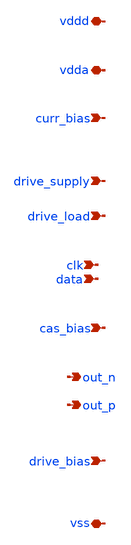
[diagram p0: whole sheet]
** sch_path: design/dac_unit_cell/dac_unit_cell_pex.sch
**.subckt dac_unit_cell_pex vdda vss curr_bias drive_supply cas_bias drive_bias drive_load vddd clk
*+ data out_p out_n
*.iopin vdda
*.iopin vss
*.ipin curr_bias
*.ipin drive_supply
*.ipin cas_bias
*.ipin drive_bias
*.ipin drive_load
*.iopin vddd
*.ipin clk
*.ipin data
*.opin out_p
*.opin out_n
**** begin user architecture code



xpex vdda curr_bias clk data out_p out_n drive_load vss drive_supply cas_bias drive_bias vddd
+ dac_unit_cell_pex_sub

* NGSPICE file created from dac_unit_cell.ext - technology: sky130A

.subckt sky130_fd_pr__nfet_01v8_lvt_0-42_8-00 a_n800_n130# a_n858_n42# a_800_n42#  w_n884_n68#
X0 a_800_n42# a_n800_n130# a_n858_n42# w_n884_n68# sky130_fd_pr__nfet_01v8_lvt ad=1.218e+11p
+ pd=1.42e+06u as=1.218e+11p ps=1.42e+06u w=420000u l=8e+06u
C0 a_800_n42# w_n884_n68# 0.03fF
C1 a_n858_n42# w_n884_n68# 0.03fF
C2 a_n800_n130# w_n884_n68# 1.73fF
.ends

.subckt sky130_fd_pr__pfet_01v8_0-84_0-15 VSUBS a_15_n84# w_n109_n184# a_n33_n181#  a_n73_n84#
X0 a_15_n84# a_n33_n181# a_n73_n84# w_n109_n184# sky130_fd_pr__pfet_01v8 ad=2.436e+11p pd=2.26e+06u
+ as=2.436e+11p ps=2.26e+06u w=840000u l=150000u
C0 a_15_n84# a_n73_n84# 0.29fF
C1 a_15_n84# a_n33_n181# 0.03fF
C2 a_n33_n181# a_n73_n84# 0.03fF
C3 a_15_n84# VSUBS 0.03fF
C4 a_n73_n84# VSUBS 0.03fF
C5 a_n33_n181# VSUBS 0.20fF
C6 w_n109_n184# VSUBS 0.24fF
.ends

.subckt sky130_fd_sc_hs__inv_1 VGND Y VPWR A VPB VNB
X0 Y A VPWR VPB sky130_fd_pr__pfet_01v8 ad=3.304e+11p pd=2.83e+06u as=3.864e+11p ps=2.93e+06u
+ w=1.12e+06u l=150000u
X1 Y A VGND VNB sky130_fd_pr__nfet_01v8_lvt ad=2.109e+11p pd=2.05e+06u as=2.627e+11p ps=2.19e+06u
+ w=740000u l=150000u
C0 VPWR VGND 0.01fF
C1 A VGND 0.08fF
C2 VPWR VPB 0.02fF
C3 Y VPWR 0.24fF
C4 Y A 0.26fF
C5 A VPWR 0.08fF
C6 Y VGND 0.19fF
C7 VGND VNB 0.37fF
C8 Y VNB 0.19fF
C9 VPWR VNB 0.36fF
C10 A VNB 0.36fF
C11 VPB VNB 0.41fF
.ends

.subckt sky130_fd_sc_hs__dfxtp_1 a_713_458# Q a_454_503# VGND a_1118_508# a_668_503#  a_206_368#
+ a_27_74# VPWR CLK a_731_101# a_561_463# VPB a_1168_124# VNB a_1210_314#  D a_1011_424#
X0 VPWR CLK a_27_74# VPB sky130_fd_pr__pfet_01v8 ad=1.50923e+12p pd=1.272e+07u as=3.304e+11p
+ ps=2.83e+06u w=1.12e+06u l=150000u
X1 a_561_463# a_206_368# a_454_503# VPB sky130_fd_pr__pfet_01v8 ad=1.967e+11p pd=2.01e+06u
+ as=1.967e+11p ps=2.01e+06u w=420000u l=150000u
X2 VPWR a_1210_314# a_1118_508# VPB sky130_fd_pr__pfet_01v8 ad=0p pd=0u as=1.995e+11p ps=1.79e+06u
+ w=420000u l=150000u
X3 a_713_458# a_561_463# VPWR VPB sky130_fd_pr__pfet_01v8 ad=4.662e+11p pd=2.79e+06u as=0p ps=0u
+ w=840000u l=150000u
X4 VPWR a_1011_424# a_1210_314# VPB sky130_fd_pr__pfet_01v8 ad=0p pd=0u as=2.478e+11p ps=2.27e+06u
+ w=840000u l=150000u
X5 Q a_1210_314# VPWR VPB sky130_fd_pr__pfet_01v8 ad=3.304e+11p pd=2.83e+06u as=0p ps=0u w=1.12e+06u
+ l=150000u
X6 Q a_1210_314# VGND VNB sky130_fd_pr__nfet_01v8_lvt ad=2.109e+11p pd=2.05e+06u as=1.27305e+12p
+ ps=1.059e+07u w=740000u l=150000u
X7 a_668_503# a_27_74# a_561_463# VPB sky130_fd_pr__pfet_01v8 ad=1.008e+11p pd=1.32e+06u as=0p ps=0u
+ w=420000u l=150000u
X8 VGND a_1011_424# a_1210_314# VNB sky130_fd_pr__nfet_01v8_lvt ad=0p pd=0u as=1.824e+11p
+ ps=1.85e+06u w=640000u l=150000u
X9 a_731_101# a_206_368# a_561_463# VNB sky130_fd_pr__nfet_01v8_lvt ad=8.82e+10p pd=1.26e+06u
+ as=1.575e+11p ps=1.73e+06u w=420000u l=150000u
X10 a_454_503# D VGND VNB sky130_fd_pr__nfet_01v8_lvt ad=3.1125e+11p pd=2.43e+06u as=0p ps=0u
+ w=420000u l=150000u
X11 a_1168_124# a_27_74# a_1011_424# VNB sky130_fd_pr__nfet_01v8_lvt ad=1.113e+11p pd=1.37e+06u
+ as=2.362e+11p ps=2.07e+06u w=420000u l=150000u
X12 a_1118_508# a_206_368# a_1011_424# VPB sky130_fd_pr__pfet_01v8 ad=0p pd=0u as=2.856e+11p
+ ps=2.45e+06u w=420000u l=150000u
X13 VPWR a_713_458# a_668_503# VPB sky130_fd_pr__pfet_01v8 ad=0p pd=0u as=0p ps=0u w=420000u
+ l=150000u
X14 VGND a_1210_314# a_1168_124# VNB sky130_fd_pr__nfet_01v8_lvt ad=0p pd=0u as=0p ps=0u w=420000u
+ l=150000u
X15 a_206_368# a_27_74# VPWR VPB sky130_fd_pr__pfet_01v8 ad=3.304e+11p pd=2.83e+06u as=0p ps=0u
+ w=1.12e+06u l=150000u
X16 a_206_368# a_27_74# VGND VNB sky130_fd_pr__nfet_01v8_lvt ad=2.553e+11p pd=2.17e+06u as=0p ps=0u
+ w=740000u l=150000u
X17 a_713_458# a_561_463# VGND VNB sky130_fd_pr__nfet_01v8_lvt ad=2.18125e+11p pd=2.05e+06u as=0p
+ ps=0u w=550000u l=150000u
X18 a_1011_424# a_27_74# a_713_458# VPB sky130_fd_pr__pfet_01v8 ad=0p pd=0u as=0p ps=0u w=840000u
+ l=150000u
X19 VGND a_713_458# a_731_101# VNB sky130_fd_pr__nfet_01v8_lvt ad=0p pd=0u as=0p ps=0u w=420000u
+ l=150000u
X20 a_1011_424# a_206_368# a_713_458# VNB sky130_fd_pr__nfet_01v8_lvt ad=0p pd=0u as=0p ps=0u
+ w=550000u l=150000u
X21 a_454_503# D VPWR VPB sky130_fd_pr__pfet_01v8 ad=0p pd=0u as=0p ps=0u w=420000u l=150000u
X22 a_561_463# a_27_74# a_454_503# VNB sky130_fd_pr__nfet_01v8_lvt ad=0p pd=0u as=0p ps=0u w=420000u
+ l=150000u
X23 VGND CLK a_27_74# VNB sky130_fd_pr__nfet_01v8_lvt ad=0p pd=0u as=2.109e+11p ps=2.05e+06u
+ w=740000u l=150000u
C0 D a_206_368# 0.42fF
C1 Q a_206_368# 0.02fF
C2 Q a_1210_314# 0.35fF
C3 D VGND 0.02fF
C4 Q VGND 0.13fF
C5 CLK a_206_368# 0.04fF
C6 VGND CLK 0.06fF
C7 a_1011_424# VPWR 0.12fF
C8 a_713_458# a_27_74# 0.59fF
C9 a_561_463# a_713_458# 0.51fF
C10 a_454_503# VPWR 0.02fF
C11 VPWR a_206_368# 1.00fF
C12 a_1210_314# VPWR 0.35fF
C13 D a_713_458# 0.02fF
C14 VGND VPWR 0.02fF
C15 a_206_368# a_1118_508# 0.03fF
C16 a_561_463# a_27_74# 0.87fF
C17 a_1011_424# a_206_368# 0.65fF
C18 a_713_458# VPWR 0.02fF
C19 a_1011_424# a_1210_314# 0.60fF
C20 a_1011_424# VGND 0.20fF
C21 a_454_503# a_206_368# 0.14fF
C22 D a_27_74# 0.20fF
C23 a_561_463# D 0.09fF
C24 VGND a_454_503# 0.02fF
C25 a_1210_314# a_206_368# 0.16fF
C26 VGND a_206_368# 0.24fF
C27 VGND a_1210_314# 0.39fF
C28 a_27_74# CLK 0.41fF
C29 VPWR VPB 0.11fF
C30 D CLK 0.02fF
C31 a_668_503# a_206_368# 0.03fF
C32 a_1011_424# a_713_458# 0.12fF
C33 a_27_74# VPWR 0.28fF
C34 a_561_463# VPWR 0.14fF
C35 a_454_503# a_713_458# 0.03fF
C36 a_713_458# a_206_368# 0.56fF
C37 a_1210_314# a_713_458# 0.03fF
C38 D VPWR 0.02fF
C39 VGND a_713_458# 0.06fF
C40 Q VPWR 0.24fF
C41 VPWR CLK 0.02fF
C42 VPB a_206_368# 0.02fF
C43 a_1011_424# a_27_74# 0.30fF
C44 a_1011_424# a_561_463# 0.03fF
C45 a_454_503# a_27_74# 0.17fF
C46 a_561_463# a_454_503# 0.34fF
C47 a_27_74# a_206_368# 1.29fF
C48 Q a_1011_424# 0.02fF
C49 a_561_463# a_206_368# 0.56fF
C50 a_1210_314# a_27_74# 0.11fF
C51 VGND a_27_74# 1.60fF
C52 a_561_463# a_1210_314# 0.03fF
C53 a_561_463# VGND 0.04fF
C54 a_731_101# a_27_74# 0.03fF
C55 D a_454_503# 0.26fF
C56 Q VNB 0.16fF
C57 a_1011_424# VNB 0.11fF
C58 VGND VNB 1.28fF
C59 a_454_503# VNB 0.12fF
C60 a_561_463# VNB 0.53fF
C61 a_713_458# VNB 0.49fF
C62 D VNB 0.39fF
C63 a_206_368# VNB 1.52fF
C64 a_27_74# VNB 1.51fF
C65 CLK VNB 0.24fF
C66 VPWR VNB 1.26fF
C67 VPB VNB 1.91fF
.ends

.subckt sky130_fd_pr__pfet_01v8_0-42_0-15_1g VSUBS a_n73_n61# w_n109_n123# a_15_n61#  a_n33_54#
X0 a_15_n61# a_n33_54# a_n73_n61# w_n109_n123# sky130_fd_pr__pfet_01v8 ad=1.218e+11p pd=1.42e+06u
+ as=1.218e+11p ps=1.42e+06u w=420000u l=150000u
C0 a_n73_n61# a_15_n61# 0.15fF
C1 a_15_n61# a_n33_54# 0.01fF
C2 a_n73_n61# a_n33_54# 0.01fF
C3 a_15_n61# VSUBS 0.03fF
C4 a_n73_n61# VSUBS 0.03fF
C5 a_n33_54# VSUBS 0.12fF
C6 w_n109_n123# VSUBS 0.16fF
.ends

.subckt sky130_fd_pr__pfet_01v8_lvt_0-55_8-00 VSUBS a_n800_n152# a_800_n55# w_n894_n155#
+  a_n858_n55#
X0 a_800_n55# a_n800_n152# a_n858_n55# w_n894_n155# sky130_fd_pr__pfet_01v8_lvt ad=1.595e+11p
+ pd=1.68e+06u as=1.595e+11p ps=1.68e+06u w=550000u l=8e+06u
C0 a_800_n55# VSUBS 0.03fF
C1 a_n858_n55# VSUBS 0.03fF
C2 a_n800_n152# VSUBS 1.82fF
C3 w_n894_n155# VSUBS 1.66fF
.ends

.subckt sky130_fd_pr__nfet_01v8_0-42_0-15_1g a_n73_n75# w_n99_n101# a_15_n75# a_n33_31#
X0 a_15_n75# a_n33_31# a_n73_n75# w_n99_n101# sky130_fd_pr__nfet_01v8 ad=1.218e+11p pd=1.42e+06u
+ as=1.218e+11p ps=1.42e+06u w=420000u l=150000u
C0 a_n33_31# a_n73_n75# 0.02fF
C1 a_15_n75# a_n73_n75# 0.15fF
C2 a_15_n75# a_n33_31# 0.02fF
C3 a_15_n75# w_n99_n101# 0.03fF
C4 a_n73_n75# w_n99_n101# 0.03fF
C5 a_n33_31# w_n99_n101# 0.12fF
.ends

.subckt sky130_fd_pr__nfet_01v8_lvt_4-00_2-00 a_200_n400# w_n284_n426# a_n200_n488#  a_n258_n400#
X0 a_200_n400# a_n200_n488# a_n258_n400# w_n284_n426# sky130_fd_pr__nfet_01v8_lvt ad=1.16e+12p
+ pd=8.58e+06u as=1.16e+12p ps=8.58e+06u w=4e+06u l=2e+06u
C0 a_200_n400# w_n284_n426# 0.03fF
C1 a_n258_n400# w_n284_n426# 0.03fF
C2 a_n200_n488# w_n284_n426# 0.51fF
.ends

.subckt sky130_fd_pr__nfet_01v8_0-84_0-15_1g a_n73_n117# w_n99_n143# a_n33_73# a_15_n117#
X0 a_15_n117# a_n33_73# a_n73_n117# w_n99_n143# sky130_fd_pr__nfet_01v8 ad=2.436e+11p pd=2.26e+06u
+ as=2.436e+11p ps=2.26e+06u w=840000u l=150000u
C0 a_n33_73# a_n73_n117# 0.02fF
C1 a_15_n117# a_n73_n117# 0.29fF
C2 a_15_n117# a_n33_73# 0.02fF
C3 a_15_n117# w_n99_n143# 0.03fF
C4 a_n73_n117# w_n99_n143# 0.03fF
C5 a_n33_73# w_n99_n143# 0.12fF
.ends



* Top level circuit dac_unit_cell
.subckt dac_unit_cell_pex_sub  vdda curr_bias clk data out_p out_n drive_load vss drive_supply
+ cas_bias   drive_bias vddd
Xsky130_fd_pr__nfet_01v8_lvt_0-42_8-00_0[0] drive_bias ctl_s vss vss
+ sky130_fd_pr__nfet_01v8_lvt_0-42_8-00
Xsky130_fd_pr__nfet_01v8_lvt_0-42_8-00_0[1] ctl_s vss vss vss sky130_fd_pr__nfet_01v8_lvt_0-42_8-00
Xsky130_fd_pr__pfet_01v8_0-84_0-15_0 vss ctl_p vdda drive_load drive_supply
+ sky130_fd_pr__pfet_01v8_0-84_0-15
Xsky130_fd_pr__pfet_01v8_0-84_0-15_1 vss ctl_n vdda drive_load drive_supply
+ sky130_fd_pr__pfet_01v8_0-84_0-15
Xsky130_fd_sc_hs__inv_1_0 vss sky130_fd_sc_hs__inv_1_0/Y vddd data vddd vss sky130_fd_sc_hs__inv_1
Xsky130_fd_sc_hs__dfxtp_1_0 sky130_fd_sc_hs__dfxtp_1_0/a_713_458# data_p
+ sky130_fd_sc_hs__dfxtp_1_0/a_454_503#  vss sky130_fd_sc_hs__dfxtp_1_0/a_1118_508# sky130_fd_sc_hs__dfxtp_1_0/a_668_503#
+  sky130_fd_sc_hs__dfxtp_1_0/a_206_368# sky130_fd_sc_hs__dfxtp_1_0/a_27_74# vddd clk  sky130_fd_sc_hs__dfxtp_1_0/a_731_101#
+ sky130_fd_sc_hs__dfxtp_1_0/a_561_463# vddd  sky130_fd_sc_hs__dfxtp_1_0/a_1168_124# vss sky130_fd_sc_hs__dfxtp_1_0/a_1210_314#  data
+ sky130_fd_sc_hs__dfxtp_1_0/a_1011_424# sky130_fd_sc_hs__dfxtp_1
Xsky130_fd_pr__pfet_01v8_0-42_0-15_1g_0 vss a_250_7220# vdda out_p cas_bias
+ sky130_fd_pr__pfet_01v8_0-42_0-15_1g
Xsky130_fd_sc_hs__dfxtp_1_1 sky130_fd_sc_hs__dfxtp_1_1/a_713_458# data_n
+ sky130_fd_sc_hs__dfxtp_1_1/a_454_503#  vss sky130_fd_sc_hs__dfxtp_1_1/a_1118_508# sky130_fd_sc_hs__dfxtp_1_1/a_668_503#
+  sky130_fd_sc_hs__dfxtp_1_1/a_206_368# sky130_fd_sc_hs__dfxtp_1_1/a_27_74# vddd clk  sky130_fd_sc_hs__dfxtp_1_1/a_731_101#
+ sky130_fd_sc_hs__dfxtp_1_1/a_561_463# vddd  sky130_fd_sc_hs__dfxtp_1_1/a_1168_124# vss sky130_fd_sc_hs__dfxtp_1_1/a_1210_314#
+  sky130_fd_sc_hs__inv_1_0/Y sky130_fd_sc_hs__dfxtp_1_1/a_1011_424# sky130_fd_sc_hs__dfxtp_1
Xpfet_01v8_lvt_0-55_8-00[0] vss curr_bias a_431_7381# vdda vdda
+ sky130_fd_pr__pfet_01v8_lvt_0-55_8-00
Xpfet_01v8_lvt_0-55_8-00[1] vss curr_bias a_431_7381# vdda vdda
+ sky130_fd_pr__pfet_01v8_lvt_0-55_8-00
Xsky130_fd_pr__pfet_01v8_0-42_0-15_1g_1 vss a_431_7381# vdda a_250_7220# ctl_p
+ sky130_fd_pr__pfet_01v8_0-42_0-15_1g
Xsky130_fd_pr__nfet_01v8_0-42_0-15_1g_0 ctl_s vss ctl_p data_p sky130_fd_pr__nfet_01v8_0-42_0-15_1g
Xsky130_fd_pr__pfet_01v8_0-42_0-15_1g_3 vss a_431_7220# vdda out_n cas_bias
+ sky130_fd_pr__pfet_01v8_0-42_0-15_1g
Xsky130_fd_pr__pfet_01v8_0-42_0-15_1g_2 vss a_431_7381# vdda a_431_7220# ctl_n
+ sky130_fd_pr__pfet_01v8_0-42_0-15_1g
Xsky130_fd_pr__nfet_01v8_lvt_4-00_2-00_0 vss vss ctl_s vss sky130_fd_pr__nfet_01v8_lvt_4-00_2-00
Xsky130_fd_pr__nfet_01v8_0-42_0-15_1g_1 ctl_s vss ctl_n data_n sky130_fd_pr__nfet_01v8_0-42_0-15_1g
Xsky130_fd_pr__nfet_01v8_0-84_0-15_1g_0 m1_97_6342# vss data_n ctl_p
+ sky130_fd_pr__nfet_01v8_0-84_0-15_1g
Xsky130_fd_pr__nfet_01v8_0-84_0-15_1g_2 ctl_n vss data_p m1_97_6342#
+ sky130_fd_pr__nfet_01v8_0-84_0-15_1g
Xsky130_fd_pr__nfet_01v8_0-84_0-15_1g_1 m1_97_6342# vss data_p ctl_n
+ sky130_fd_pr__nfet_01v8_0-84_0-15_1g
Xsky130_fd_pr__nfet_01v8_0-84_0-15_1g_3 ctl_p vss data_n m1_97_6342#
+ sky130_fd_pr__nfet_01v8_0-84_0-15_1g
C0 m3_49_1697# sky130_fd_sc_hs__dfxtp_1_1/a_561_463# 0.09fF
C1 clk m3_49_n990# 0.12fF
C2 a_501_5998# ctl_s 0.02fF
C3 m3_49_1697# sky130_fd_sc_hs__dfxtp_1_1/a_27_74# 0.06fF
C4 ctl_p a_179_5998# 0.05fF
C5 a_431_7381# out_n 0.04fF
C6 ctl_p m1_97_6342# 0.23fF
C7 ctl_n drive_supply 0.20fF
C8 sky130_fd_sc_hs__dfxtp_1_0/a_1011_424# sky130_fd_sc_hs__inv_1_0/Y 0.06fF
C9 drive_bias ctl_s 0.19fF
C10 m3_49_552# sky130_fd_sc_hs__inv_1_0/Y 0.14fF
C11 m3_49_1697# sky130_fd_sc_hs__dfxtp_1_1/a_713_458# 0.21fF
C12 ctl_p vdda 0.03fF
C13 m3_49_832# data_p 0.32fF
C14 vddd data_n 0.15fF
C15 sky130_fd_sc_hs__dfxtp_1_0/a_1210_314# clk 0.20fF
C16 drive_load ctl_n 0.68fF
C17 ctl_p out_n 0.16fF
C18 ctl_p a_431_7381# 0.05fF
C19 sky130_fd_sc_hs__dfxtp_1_1/a_206_368# vddd 0.02fF
C20 sky130_fd_sc_hs__dfxtp_1_0/a_561_463# clk 0.13fF
C21 sky130_fd_sc_hs__dfxtp_1_0/a_713_458# sky130_fd_sc_hs__inv_1_0/Y 0.06fF
C22 ctl_n data_p 0.23fF
C23 drive_supply m1_97_6342# 0.10fF
C24 data vddd 0.28fF
C25 sky130_fd_sc_hs__dfxtp_1_0/a_206_368# clk 0.24fF
C26 curr_bias ctl_n 0.01fF
C27 vdda drive_supply 0.04fF
C28 cas_bias a_250_7220# 0.01fF
C29 sky130_fd_sc_hs__dfxtp_1_0/a_27_74# sky130_fd_sc_hs__inv_1_0/Y 0.47fF
C30 sky130_fd_sc_hs__dfxtp_1_0/a_1118_508# sky130_fd_sc_hs__inv_1_0/Y 0.04fF
C31 drive_load m1_97_6342# 0.02fF
C32 ctl_s data_p 1.37fF
C33 out_n drive_supply 0.46fF
C34 a_250_7220# a_431_7220# 0.09fF
C35 sky130_fd_sc_hs__inv_1_0/Y m3_49_n710# 0.18fF
C36 cas_bias out_p 0.40fF
C37 sky130_fd_sc_hs__dfxtp_1_1/a_561_463# data_p 0.07fF
C38 m3_49_832# vddd 0.19fF
C39 sky130_fd_sc_hs__dfxtp_1_1/a_27_74# data_p 0.62fF
C40 vddd m3_49_n990# 0.24fF
C41 ctl_n data_n 0.09fF
C42 drive_load vdda 0.01fF
C43 sky130_fd_sc_hs__dfxtp_1_0/a_668_503# sky130_fd_sc_hs__inv_1_0/Y 0.02fF
C44 m3_49_1977# sky130_fd_sc_hs__dfxtp_1_1/a_27_74# 0.08fF
C45 sky130_fd_sc_hs__dfxtp_1_0/a_1011_424# clk 0.11fF
C46 a_179_5998# data_p 0.02fF
C47 cas_bias a_431_7220# 0.01fF
C48 drive_load out_n 0.36fF
C49 m3_49_552# clk 0.14fF
C50 data_p m1_97_6342# 0.22fF
C51 sky130_fd_sc_hs__dfxtp_1_1/a_206_368# sky130_fd_sc_hs__dfxtp_1_0/a_1210_314# 0.02fF
C52 sky130_fd_sc_hs__dfxtp_1_1/a_713_458# data_p 0.14fF
C53 data m3_49_n990# 0.38fF
C54 ctl_p drive_supply 0.20fF
C55 ctl_s data_n 3.06fF
C56 clk sky130_fd_sc_hs__inv_1_0/Y 0.62fF
C57 ctl_n a_250_7220# 0.01fF
C58 sky130_fd_sc_hs__dfxtp_1_0/a_27_74# m3_49_n710# 0.29fF
C59 ctl_p drive_load 0.68fF
C60 curr_bias vdda 0.23fF
C61 ctl_n out_p 0.13fF
C62 sky130_fd_sc_hs__dfxtp_1_0/a_713_458# clk 0.04fF
C63 sky130_fd_sc_hs__dfxtp_1_1/a_454_503# data_p 0.08fF
C64 ctl_n cas_bias 0.24fF
C65 data_n m1_97_6342# 0.22fF
C66 data_p sky130_fd_sc_hs__inv_1_0/Y 0.18fF
C67 m3_49_1697# sky130_fd_sc_hs__dfxtp_1_1/a_731_101# 0.02fF
C68 curr_bias a_431_7381# 0.12fF
C69 ctl_n a_431_7220# 0.04fF
C70 m3_49_832# sky130_fd_sc_hs__dfxtp_1_0/a_1210_314# 0.25fF
C71 sky130_fd_sc_hs__dfxtp_1_1/a_27_74# vddd 0.05fF
C72 ctl_p data_p 0.10fF
C73 sky130_fd_sc_hs__dfxtp_1_0/a_206_368# vddd 0.02fF
C74 sky130_fd_sc_hs__dfxtp_1_0/a_27_74# clk 0.14fF
C75 m3_49_1697# data_p 0.14fF
C76 m3_49_1977# m3_49_1697# 0.52fF
C77 clk m3_49_n710# 0.25fF
C78 ctl_p curr_bias 0.01fF
C79 data sky130_fd_sc_hs__dfxtp_1_0/a_206_368# 0.09fF
C80 drive_load drive_supply 0.14fF
C81 drive_bias data_p 1.60fF
C82 sky130_fd_sc_hs__dfxtp_1_1/a_1168_124# data_p 0.01fF
C83 m3_49_552# vddd 0.37fF
C84 m3_49_832# sky130_fd_sc_hs__dfxtp_1_1/a_27_74# 0.10fF
C85 ctl_p data_n 0.16fF
C86 vdda out_p 0.01fF
C87 sky130_fd_sc_hs__dfxtp_1_1/a_206_368# sky130_fd_sc_hs__inv_1_0/Y 0.16fF
C88 vdda cas_bias 0.04fF
C89 data_p drive_supply 0.01fF
C90 vddd sky130_fd_sc_hs__inv_1_0/Y 0.62fF
C91 out_n out_p 0.73fF
C92 sky130_fd_sc_hs__dfxtp_1_1/a_1210_314# data_p 0.44fF
C93 sky130_fd_sc_hs__dfxtp_1_0/a_454_503# sky130_fd_sc_hs__inv_1_0/Y 0.04fF
C94 out_n cas_bias 0.33fF
C95 m3_49_1977# sky130_fd_sc_hs__dfxtp_1_1/a_1210_314# 0.17fF
C96 a_431_7381# out_p 0.04fF
C97 a_501_5998# data_n 0.02fF
C98 a_431_7381# cas_bias 0.06fF
C99 sky130_fd_sc_hs__dfxtp_1_1/a_27_74# sky130_fd_sc_hs__dfxtp_1_0/a_1210_314# 0.09fF
C100 drive_bias data_n 0.08fF
C101 ctl_p a_250_7220# 0.04fF
C102 m3_49_1697# sky130_fd_sc_hs__dfxtp_1_1/a_206_368# 0.15fF
C103 drive_load data_p 0.01fF
C104 data sky130_fd_sc_hs__inv_1_0/Y 0.47fF
C105 m3_49_552# m3_49_832# 0.52fF
C106 data_p clk 0.31fF
C107 m3_49_1697# vddd 0.24fF
C108 ctl_n m1_97_6342# 0.23fF
C109 ctl_p out_p 0.19fF
C110 data_p sky130_fd_sc_hs__dfxtp_1_1/a_1011_424# 0.20fF
C111 ctl_p cas_bias 0.24fF
C112 data_n drive_supply 0.01fF
C113 m3_49_1977# sky130_fd_sc_hs__dfxtp_1_1/a_1011_424# 0.22fF
C114 m3_49_832# sky130_fd_sc_hs__inv_1_0/Y 0.14fF
C115 sky130_fd_sc_hs__dfxtp_1_0/a_27_74# vddd 0.06fF
C116 sky130_fd_sc_hs__inv_1_0/Y m3_49_n990# 0.21fF
C117 ctl_n vdda 0.03fF
C118 ctl_p a_431_7220# 0.01fF
C119 m3_49_552# sky130_fd_sc_hs__dfxtp_1_0/a_1210_314# 0.19fF
C120 m3_49_1977# data_p 0.18fF
C121 ctl_s a_179_5998# 0.03fF
C122 vddd m3_49_n710# 0.22fF
C123 ctl_s m1_97_6342# 0.07fF
C124 ctl_n out_n 0.28fF
C125 drive_load data_n 0.02fF
C126 ctl_n a_431_7381# 0.05fF
C127 data sky130_fd_sc_hs__dfxtp_1_0/a_27_74# 0.14fF
C128 sky130_fd_sc_hs__dfxtp_1_0/a_1210_314# sky130_fd_sc_hs__inv_1_0/Y 0.06fF
C129 a_250_7220# drive_supply 0.01fF
C130 sky130_fd_sc_hs__dfxtp_1_1/a_1210_314# vddd 0.01fF
C131 data m3_49_n710# 0.14fF
C132 out_p drive_supply 0.03fF
C133 data_p data_n 2.90fF
C134 ctl_p ctl_n 0.15fF
C135 sky130_fd_sc_hs__dfxtp_1_1/a_27_74# sky130_fd_sc_hs__dfxtp_1_0/a_1011_424# 0.02fF
C136 cas_bias drive_supply 0.94fF
C137 m3_49_1977# data_n 0.02fF
C138 sky130_fd_sc_hs__dfxtp_1_0/a_561_463# sky130_fd_sc_hs__inv_1_0/Y 0.06fF
C139 clk vddd 0.04fF
C140 sky130_fd_sc_hs__dfxtp_1_0/a_454_503# clk 0.03fF
C141 m3_49_n990# m3_49_n710# 0.52fF
C142 drive_supply a_431_7220# 0.01fF
C143 drive_load out_p 0.12fF
C144 sky130_fd_sc_hs__dfxtp_1_1/a_206_368# data_p 0.15fF
C145 ctl_n a_501_5998# 0.05fF
C146 drive_load cas_bias 0.05fF
C147 data clk 0.88fF
C148 sky130_fd_sc_hs__dfxtp_1_1/a_27_74# sky130_fd_sc_hs__inv_1_0/Y 0.08fF
C149 m3_49_1977# sky130_fd_sc_hs__dfxtp_1_1/a_206_368# 0.14fF
C150 sky130_fd_sc_hs__dfxtp_1_0/a_206_368# sky130_fd_sc_hs__inv_1_0/Y 0.44fF
C151 data_p vddd 0.19fF
C152 m3_49_1977# vddd 0.25fF
C153 vdda out_n 0.01fF
C154 m3_49_552# sky130_fd_sc_hs__dfxtp_1_0/a_1011_424# 0.08fF
C155 m3_49_832# clk 0.43fF
C156 m3_49_n990# vss 0.13fF $ **FLOATING
C157 m3_49_n710# vss 0.18fF $ **FLOATING
C158 m3_49_552# vss 0.28fF $ **FLOATING
C159 m3_49_832# vss 0.02fF $ **FLOATING
C160 m3_49_1697# vss 0.30fF $ **FLOATING
C161 m3_49_1977# vss 0.41fF $ **FLOATING
C162 ctl_n vss 0.19fF
C163 ctl_p vss 0.85fF
C164 m1_97_6342# vss 0.37fF
C165 a_250_7220# vss 0.03fF
C166 curr_bias vss 18.15fF
C167 a_501_5998# vss 1.00fF $ **FLOATING
C168 a_179_5998# vss 1.00fF $ **FLOATING
C169 drive_load vss 0.89fF
C170 a_431_7220# vss 0.03fF
C171 a_431_7381# vss 0.17fF
C172 out_n vss 0.37fF
C173 data_n vss 0.75fF
C174 sky130_fd_sc_hs__dfxtp_1_1/a_1011_424# vss 0.11fF
C175 sky130_fd_sc_hs__dfxtp_1_1/a_454_503# vss 0.12fF
C176 sky130_fd_sc_hs__dfxtp_1_1/a_1210_314# vss 0.04fF
C177 sky130_fd_sc_hs__dfxtp_1_1/a_561_463# vss 0.53fF
C178 sky130_fd_sc_hs__dfxtp_1_1/a_713_458# vss 0.49fF
C179 sky130_fd_sc_hs__dfxtp_1_1/a_206_368# vss 1.52fF
C180 sky130_fd_sc_hs__dfxtp_1_1/a_27_74# vss 1.55fF
C181 out_p vss 0.46fF
C182 cas_bias vss 0.11fF
C183 data_p vss 0.49fF
C184 sky130_fd_sc_hs__dfxtp_1_0/a_1011_424# vss 0.11fF
C185 sky130_fd_sc_hs__dfxtp_1_0/a_454_503# vss 0.12fF
C186 sky130_fd_sc_hs__dfxtp_1_0/a_1210_314# vss 0.02fF
C187 sky130_fd_sc_hs__dfxtp_1_0/a_561_463# vss 0.53fF
C188 sky130_fd_sc_hs__dfxtp_1_0/a_713_458# vss 0.49fF
C189 data vss 1.37fF
C190 sky130_fd_sc_hs__dfxtp_1_0/a_206_368# vss 1.53fF
C191 sky130_fd_sc_hs__dfxtp_1_0/a_27_74# vss 1.57fF
C192 clk vss 0.71fF
C193 vddd vss 8.09fF
C194 sky130_fd_sc_hs__inv_1_0/Y vss 0.60fF
C195 drive_supply vss 0.36fF
C196 vdda vss 5.89fF
C197 ctl_s vss 0.45fF
C198 drive_bias vss 1.93fF
.ends
.end




**** end user architecture code
**.ends
.end
